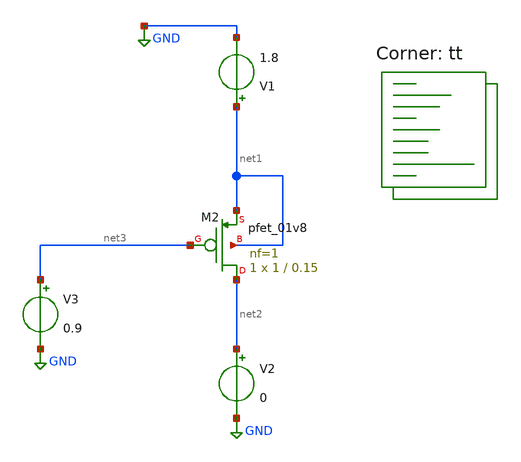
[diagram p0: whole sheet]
** sch_path: xschem/Verif_1.sch
**.subckt Verif_1
XM2 net2 net3 net1 net1 sky130_fd_pr__pfet_01v8 L=0.15 W=1 nf=1 ad='int((nf+1)/2) * W/nf * 0.29' as='int((nf+2)/2) * W/nf * 0.29'
+ pd='2*int((nf+1)/2) * (W/nf + 0.29)' ps='2*int((nf+2)/2) * (W/nf + 0.29)' nrd='0.29 / W' nrs='0.29 / W'
+ sa=0 sb=0 sd=0 mult=1 m=1
V1 net1 GND 1.8
V2 net2 GND 0
V3 net3 GND 0.9
**** begin user architecture code
.lib $::SKYWATER_MODELS/sky130.lib.spice tt


.option savecurrents

.control
save all


save @m.xm2.msky130_fd_pr__pfet_01v8[id]
save @m.xm2.msky130_fd_pr__pfet_01v8[gm]
save @m.xm2.msky130_fd_pr__pfet_01v8[gds]
save @m.xm2.msky130_fd_pr__pfet_01v8[vth]
save @m.xm2.msky130_fd_pr__pfet_01v8[cgg]
save @m.xm2.msky130_fd_pr__pfet_01v8[vds]
save @m.xm2.msky130_fd_pr__pfet_01v8[vgs]
save @m.xm2.msky130_fd_pr__pfet_01v8[vbs]
save @m.xm2.msky130_fd_pr__pfet_01v8[l]

foreach l_act 0.15 0.45 0.75 1 2 3 4 5 8 10
  alter @m.xm2.msky130_fd_pr__pfet_01v8[l] = $l_act
  dc V2 0 1.8 0.02 V3 0 1.8 0.02
end
  plot all.@m.xm2.msky130_fd_pr__pfet_01v8[gm]
  plot all.@m.xm2.msky130_fd_pr__pfet_01v8[gds]
  plot all.@m.xm2.msky130_fd_pr__pfet_01v8[vth]
  plot all.@m.xm2.msky130_fd_pr__pfet_01v8[cgg]
  plot all.@m.xm2.msky130_fd_pr__pfet_01v8[id]
  plot all.@m.xm2.msky130_fd_pr__pfet_01v8[vbs]
  plot all.@m.xm2.msky130_fd_pr__pfet_01v8[vgs]
  plot all.@m.xm2.msky130_fd_pr__pfet_01v8[vds]
  set appendwrite
set filetype=binary
write GmId.raw

set wr_vecnames
wrdata GmIdp.csv all.@m.xm2.msky130_fd_pr__pfet_01v8[id] all.@m.xm2.msky130_fd_pr__pfet_01v8[gm]
+  all.@m.xm2.msky130_fd_pr__pfet_01v8[gds] all.@m.xm2.msky130_fd_pr__pfet_01v8[cgg] all.@m.xm2.msky130_fd_pr__pfet_01v8[vds]
+ all.@m.xm2.msky130_fd_pr__pfet_01v8[vgs] all.@m.xm2.msky130_fd_pr__pfet_01v8[vth]
.endc



**** end user architecture code
**.ends
.GLOBAL GND
.end
